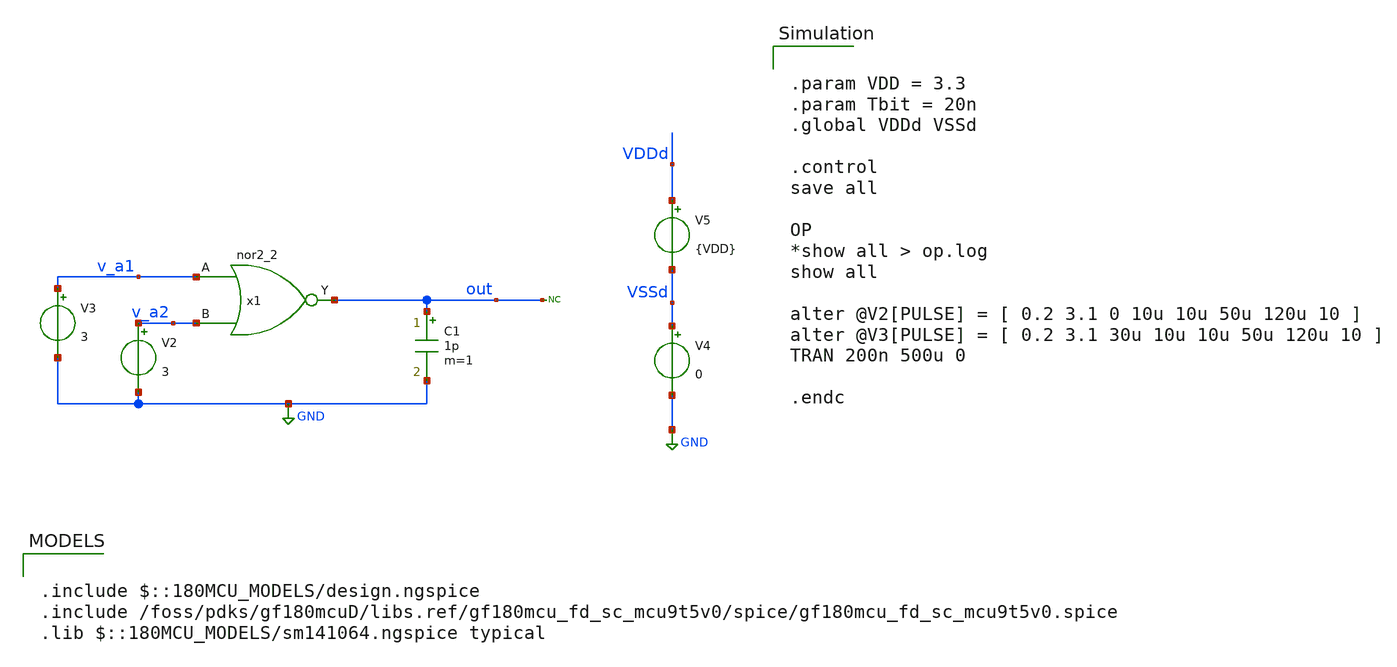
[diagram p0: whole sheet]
** sch_path: designs/switch_matrix_gf180mcu_9t5v0-main/designs/libs/tb_digital/test_digital_tb.sch
**.subckt test_digital_tb
* noconn out
V2 v_a2 GND 3
V3 v_a1 GND 3
V4 VSSd GND 0
V5 VDDd VSSd {VDD}
C1 out GND 1p m=1
x1 v_a1 v_a2 VSSd VDDd VSSd VDDd out gf180mcu_fd_sc_mcu9t5v0__nor2_2
**** begin user architecture code

.include $::180MCU_MODELS/design.ngspice
.include /foss/pdks/gf180mcuD/libs.ref/gf180mcu_fd_sc_mcu9t5v0/spice/gf180mcu_fd_sc_mcu9t5v0.spice
.lib $::180MCU_MODELS/sm141064.ngspice typical



.param VDD = 3.3
.param Tbit = 20n
.global VDDd VSSd

.control
save all

OP
*show all > op.log
show all

alter @V2[PULSE] = [ 0.2 3.1 0 10u 10u 50u 120u 10 ]
alter @V3[PULSE] = [ 0.2 3.1 30u 10u 10u 50u 120u 10 ]
TRAN 200n 500u 0

.endc


**** end user architecture code
**.ends
.GLOBAL GND
.end
